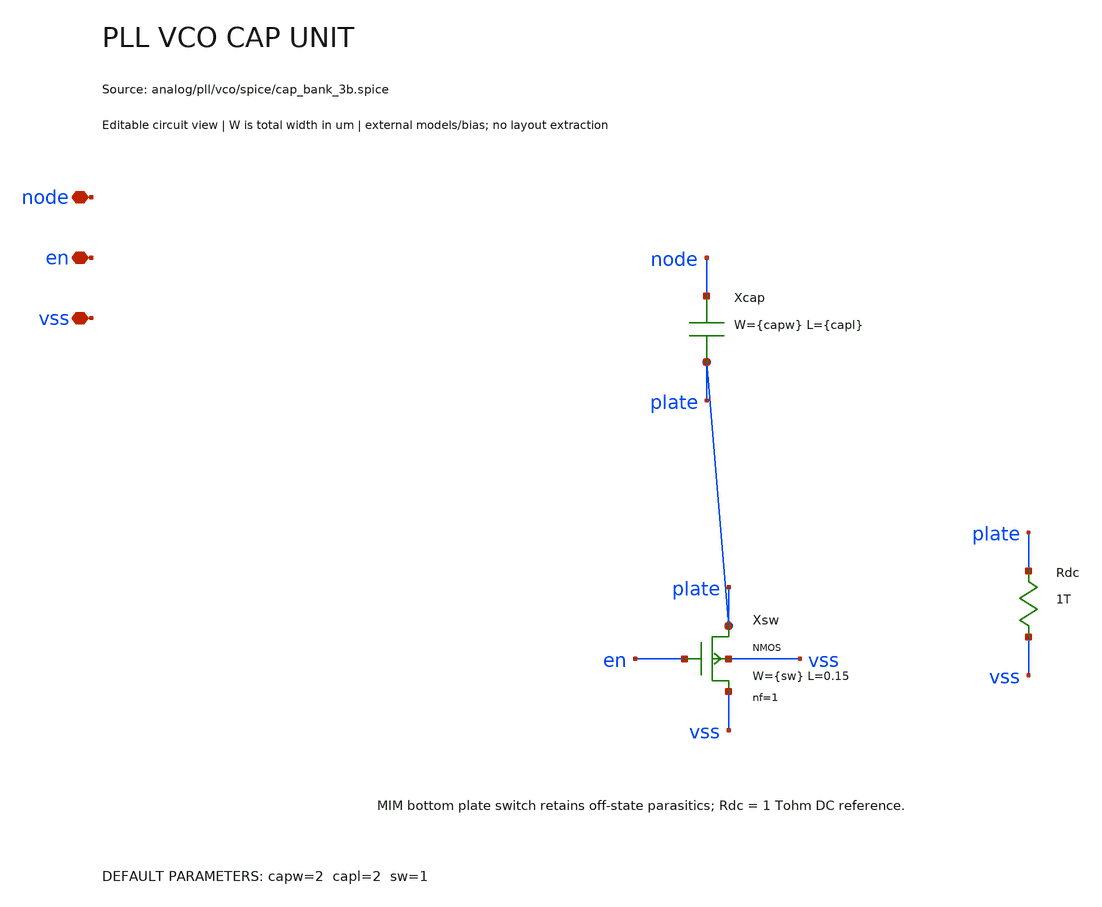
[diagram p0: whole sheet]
** sch_path: analog/pll/vco/schematic/pll_vco_cap_unit.sch
**.subckt pll_vco_cap_unit node en vss
*.iopin node
*.iopin en
*.iopin vss
Xcap node plate sky130_fd_pr__cap_mim_m3_1 w={capw} l={capl}
Xsw plate en vss vss sky130_fd_pr__nfet_01v8 w={sw} l=0.15 nf=1 ad={sw*0.29} as={sw*0.29} pd={2*(sw+0.29)}
+ ps={2*(sw+0.29)}
Rdc plate vss 1T
**.ends
.end
